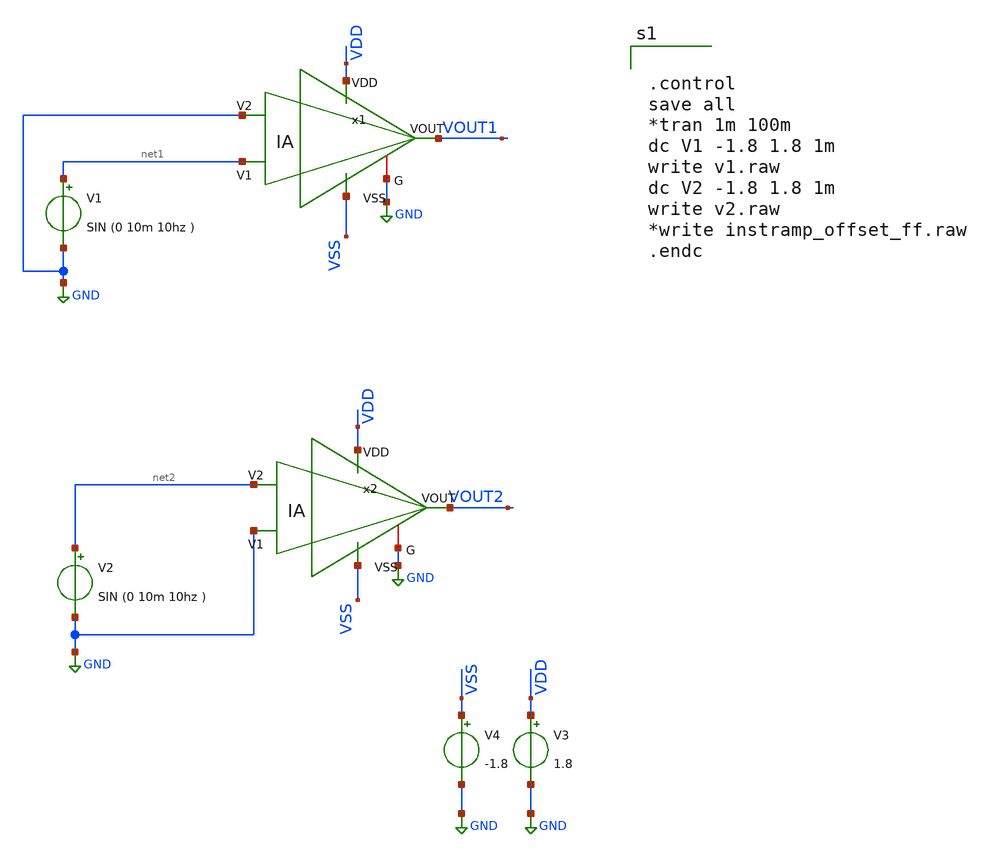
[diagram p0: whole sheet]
** sch_path: xschem/instramp_offset_ff.sch
**.subckt instramp_offset_ff
V1 net1 GND SIN (0 10m 10hz )
V2 net2 GND SIN (0 10m 10hz )
V4 VSS GND -1.8
V3 VDD GND 1.8
x1 VDD VSS VOUT1 net1 GND GND IA
x2 VDD VSS VOUT2 GND net2 GND IA
**** begin user architecture code

** opencircuitdesign pdks install
.lib $::SKYWATER_MODELS/sky130.lib.spice ff




.control
save all
*tran 1m 100m
dc V1 -1.8 1.8 1m
write v1.raw
dc V2 -1.8 1.8 1m
write v2.raw
*write instramp_offset_ff.raw
.endc


**** end user architecture code
**.ends

* expanding   symbol:  /foss/designs/chipalooza2024/sky130_hcmus_ip__instramp/xschem/IA.sym # of
*+ pins=6
** sym_path: /foss/designs/chipalooza2024/sky130_hcmus_ip__instramp/xschem/IA.sym
** sch_path: /foss/designs/chipalooza2024/sky130_hcmus_ip__instramp/xschem/IA.sch
.subckt IA VDD VSS VOUT V1 V2 G
*.opin VOUT
*.iopin G
*.ipin VDD
*.ipin VSS
*.ipin V1
*.ipin V2
XR1 net9 VOUT VSS sky130_fd_pr__res_high_po W=1 L=62 mult=1 m=1
XR4 net8 net1 VSS sky130_fd_pr__res_high_po W=1 L=62 mult=1 m=1
XR6 net12 G VSS sky130_fd_pr__res_high_po W=1 L=62 mult=1 m=1
XR8 net11 net2 VSS sky130_fd_pr__res_high_po W=1 L=62 mult=1 m=1
XR9 net3 net7 VSS sky130_fd_pr__res_high_po W=1 L=62 mult=1 m=1
XR12 net10 net4 VSS sky130_fd_pr__res_high_po W=1 L=62 mult=1 m=1
XR13 net5 net6 VSS sky130_fd_pr__res_high_po W=1 L=62 mult=1 m=1
x1 VDD VSS V2 net5 net3 opamp
x2 VDD VSS V1 net6 net4 opamp
x3 VDD VSS net2 net1 VOUT opamp
XR2 net7 net5 VSS sky130_fd_pr__res_high_po W=1 L=62 mult=1 m=1
XR3 net3 net8 VSS sky130_fd_pr__res_high_po W=1 L=62 mult=1 m=1
XR5 net1 net9 VSS sky130_fd_pr__res_high_po W=1 L=62 mult=1 m=1
XR7 net6 net10 VSS sky130_fd_pr__res_high_po W=1 L=62 mult=1 m=1
XR10 net4 net11 VSS sky130_fd_pr__res_high_po W=1 L=62 mult=1 m=1
XR11 net2 net12 VSS sky130_fd_pr__res_high_po W=1 L=62 mult=1 m=1
.ends


* expanding   symbol:  /foss/designs/chipalooza2024/sky130_hcmus_ip__instramp/xschem/opamp.sym # of
*+ pins=5
** sym_path: /foss/designs/chipalooza2024/sky130_hcmus_ip__instramp/xschem/opamp.sym
** sch_path: /foss/designs/chipalooza2024/sky130_hcmus_ip__instramp/xschem/opamp.sch
.subckt opamp VDD VSS V1 V2 VOUT
*.ipin VSS
*.ipin VDD
*.ipin V2
*.ipin V1
*.opin VOUT
XM2 net5 V2 net1 VSS sky130_fd_pr__nfet_g5v0d10v5 L=1 W=18 nf=1 ad='int((nf+1)/2) * W/nf * 0.29' as='int((nf+2)/2) * W/nf * 0.29'
+ pd='2*int((nf+1)/2) * (W/nf + 0.29)' ps='2*int((nf+2)/2) * (W/nf + 0.29)' nrd='0.29 / W' nrs='0.29 / W'
+ sa=0 sb=0 sd=0 mult=1 m=1
XM1 net6 net5 VDD VDD sky130_fd_pr__pfet_g5v0d10v5 L=1 W=30 nf=1 ad='int((nf+1)/2) * W/nf * 0.29' as='int((nf+2)/2) * W/nf * 0.29'
+ pd='2*int((nf+1)/2) * (W/nf + 0.29)' ps='2*int((nf+2)/2) * (W/nf + 0.29)' nrd='0.29 / W' nrs='0.29 / W'
+ sa=0 sb=0 sd=0 mult=1 m=1
XM4 net6 V1 net1 VSS sky130_fd_pr__nfet_g5v0d10v5 L=1 W=18 nf=1 ad='int((nf+1)/2) * W/nf * 0.29' as='int((nf+2)/2) * W/nf * 0.29'
+ pd='2*int((nf+1)/2) * (W/nf + 0.29)' ps='2*int((nf+2)/2) * (W/nf + 0.29)' nrd='0.29 / W' nrs='0.29 / W'
+ sa=0 sb=0 sd=0 mult=1 m=1
XM5 net1 net4 VSS VSS sky130_fd_pr__nfet_g5v0d10v5 L=1 W=15.171 nf=1 ad='int((nf+1)/2) * W/nf * 0.29'
+ as='int((nf+2)/2) * W/nf * 0.29' pd='2*int((nf+1)/2) * (W/nf + 0.29)' ps='2*int((nf+2)/2) * (W/nf + 0.29)'
+ nrd='0.29 / W' nrs='0.29 / W' sa=0 sb=0 sd=0 mult=1 m=1
XM6 VOUT net4 VSS VSS sky130_fd_pr__nfet_g5v0d10v5 L=1 W=19 nf=1 ad='int((nf+1)/2) * W/nf * 0.29' as='int((nf+2)/2) * W/nf * 0.29'
+ pd='2*int((nf+1)/2) * (W/nf + 0.29)' ps='2*int((nf+2)/2) * (W/nf + 0.29)' nrd='0.29 / W' nrs='0.29 / W'
+ sa=0 sb=0 sd=0 mult=1 m=1
XM7 net4 net4 VSS VSS sky130_fd_pr__nfet_g5v0d10v5 L=1 W=20 nf=1 ad='int((nf+1)/2) * W/nf * 0.29' as='int((nf+2)/2) * W/nf * 0.29'
+ pd='2*int((nf+1)/2) * (W/nf + 0.29)' ps='2*int((nf+2)/2) * (W/nf + 0.29)' nrd='0.29 / W' nrs='0.29 / W'
+ sa=0 sb=0 sd=0 mult=1 m=1
XM3 net5 net5 VDD VDD sky130_fd_pr__pfet_g5v0d10v5 L=1 W=30 nf=1 ad='int((nf+1)/2) * W/nf * 0.29' as='int((nf+2)/2) * W/nf * 0.29'
+ pd='2*int((nf+1)/2) * (W/nf + 0.29)' ps='2*int((nf+2)/2) * (W/nf + 0.29)' nrd='0.29 / W' nrs='0.29 / W'
+ sa=0 sb=0 sd=0 mult=1 m=1
XM8 VOUT net6 VDD VDD sky130_fd_pr__pfet_g5v0d10v5 L=1 W=38 nf=1 ad='int((nf+1)/2) * W/nf * 0.29' as='int((nf+2)/2) * W/nf * 0.29'
+ pd='2*int((nf+1)/2) * (W/nf + 0.29)' ps='2*int((nf+2)/2) * (W/nf + 0.29)' nrd='0.29 / W' nrs='0.29 / W'
+ sa=0 sb=0 sd=0 mult=2 m=2
XR3 net2 VDD VSS sky130_fd_pr__res_high_po W=1 L=30 mult=1 m=1
XR1 net3 net2 VSS sky130_fd_pr__res_high_po W=1 L=30 mult=1 m=1
XR2 net4 net3 VSS sky130_fd_pr__res_high_po W=1 L=30 mult=1 m=1
XR4 net7 VOUT VSS sky130_fd_pr__res_high_po W=1 L=5 mult=1 m=1
XC1 net7 net6 sky130_fd_pr__cap_mim_m3_1 W=5.5 L=10 MF=10 m=10
.ends

.GLOBAL GND
.end
